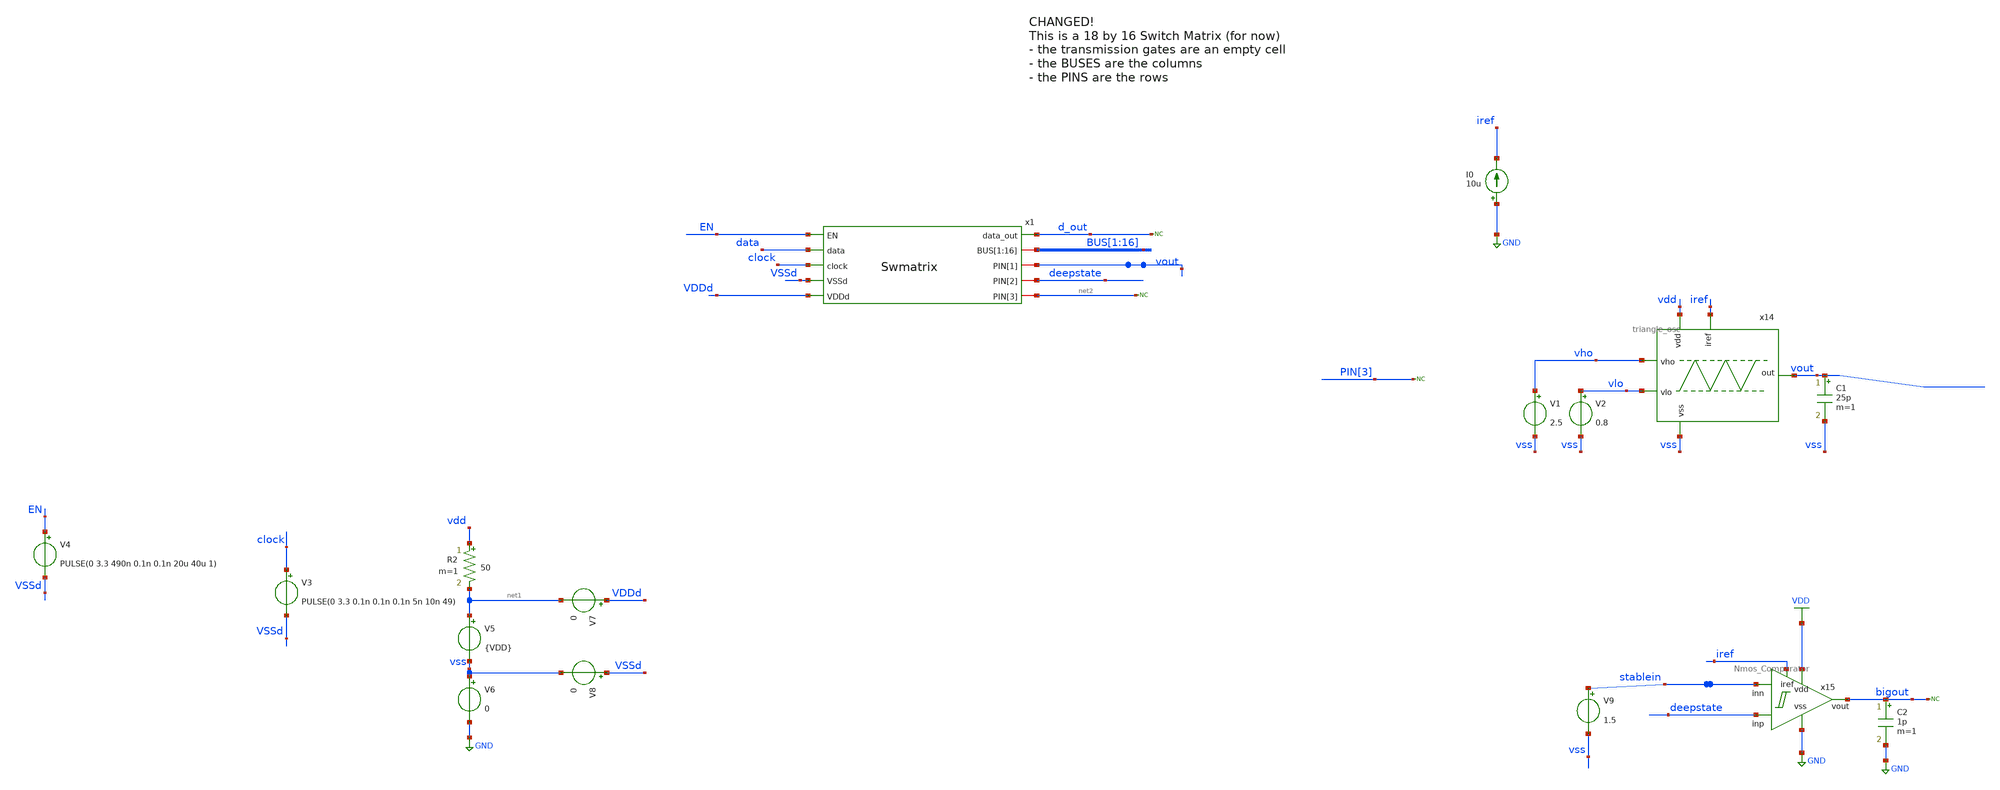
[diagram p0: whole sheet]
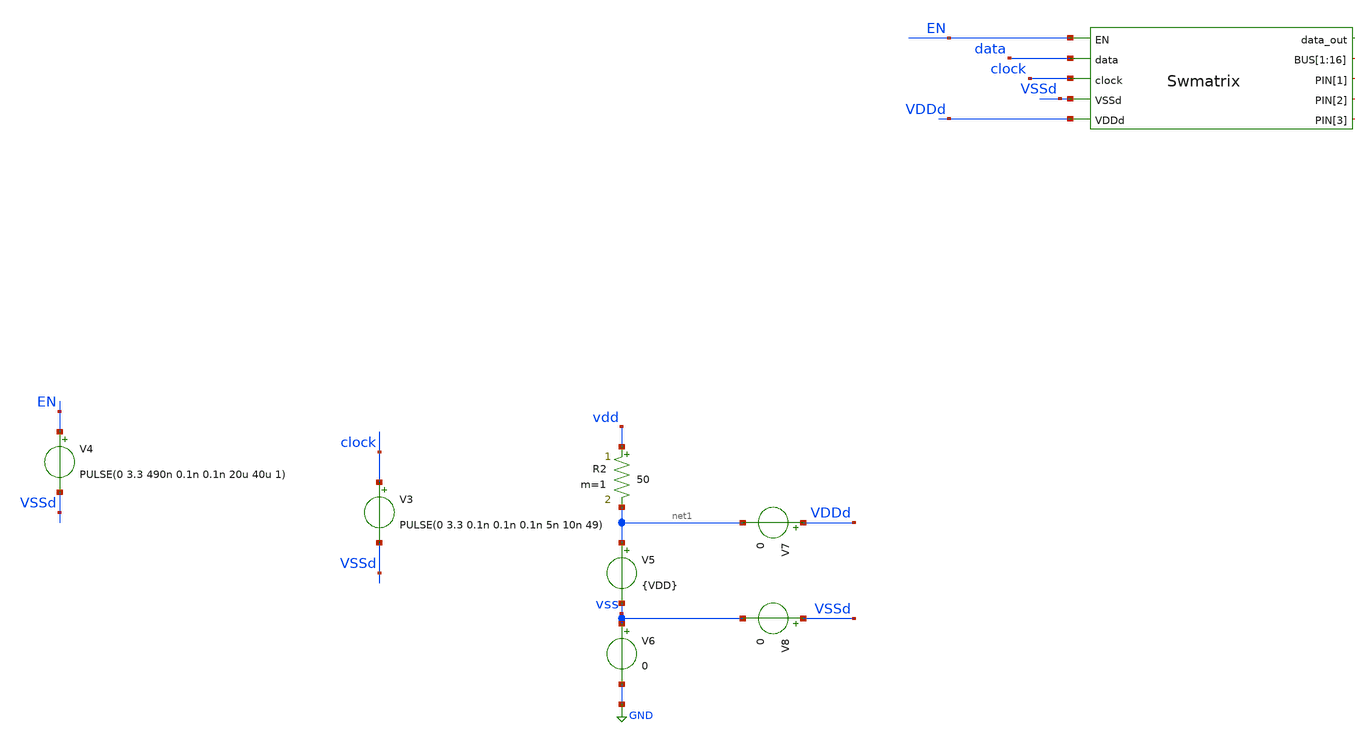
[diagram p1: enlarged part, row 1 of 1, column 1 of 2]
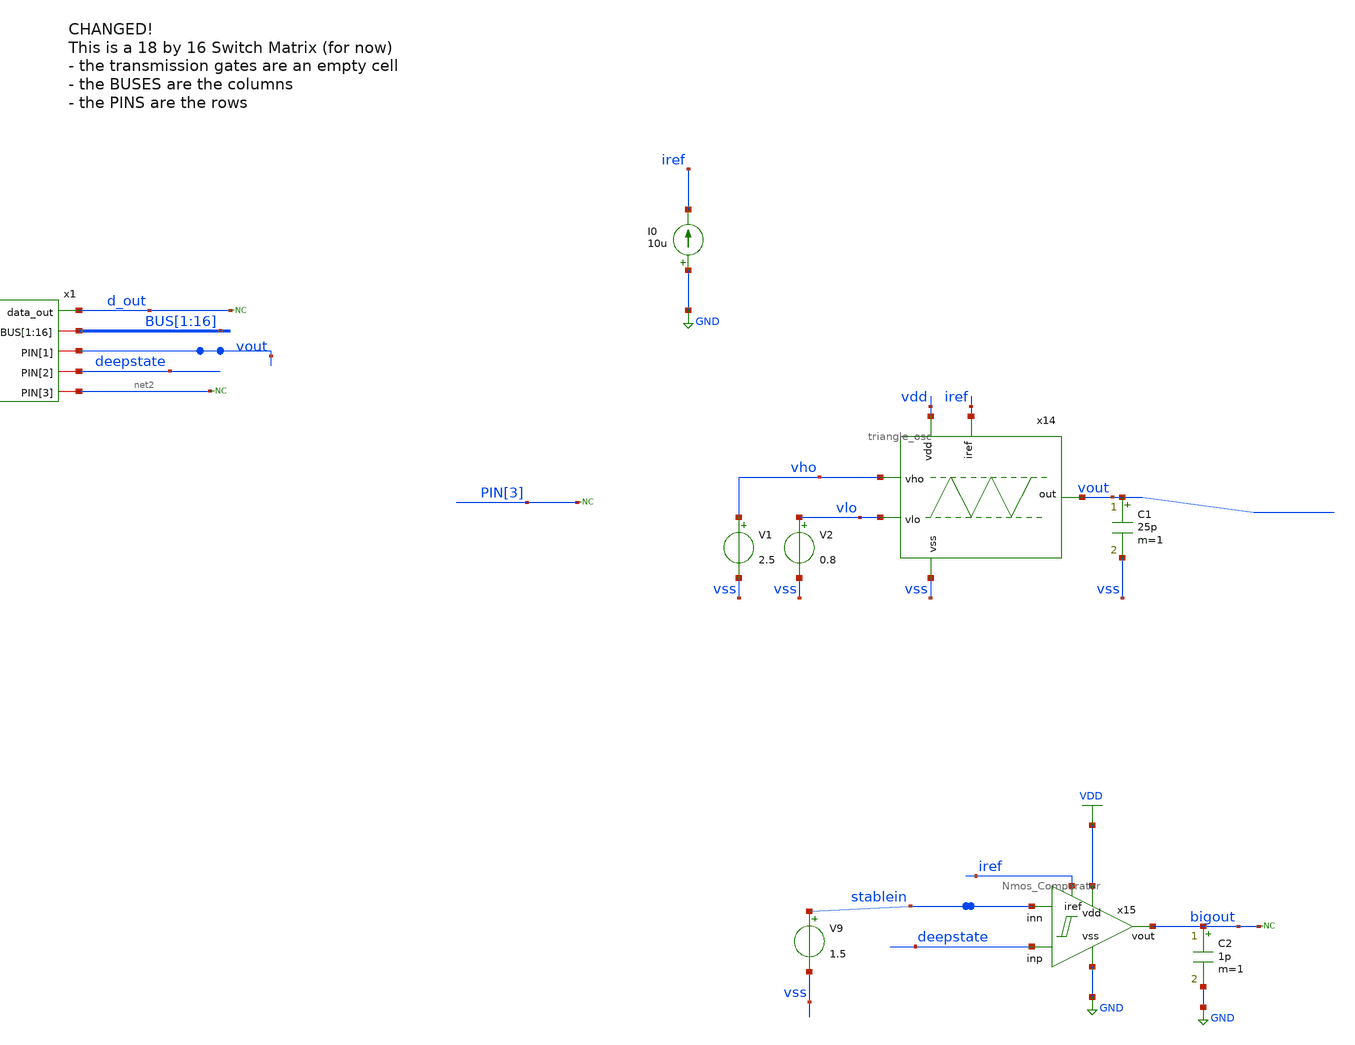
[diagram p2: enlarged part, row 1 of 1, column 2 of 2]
** sch_path: designs/savestate.sch
**.subckt savestate
* noconn d_out
V3 clock VSSd PULSE(0 3.3 0.1n 0.1n 0.1n 5n 10n 49)
V4 EN VSSd PULSE(0 3.3 490n 0.1n 0.1n 20u 40u 1)
V5 net1 vss {VDD}
V6 vss GND 0
V7 VDDd net1 0
V8 VSSd vss 0
R2 vdd net1 50 m=1
* noconn PIN[3]
x14 vdd vho vout vlo iref vss triangle_osc
V1 vho vss 2.5
V2 vlo vss 0.8
C1 vout vss 25p m=1
I0 GND iref 10u
* noconn bigout
x15 VDD bigout deepstate GND stablein iref Nmos_Comparator
C2 bigout GND 1p m=1
V9 stablein vss 1.5
x1 EN data d_out BUS[1] BUS[2] BUS[3] BUS[4] BUS[5] BUS[6] BUS[7] BUS[8] BUS[9] BUS[10] BUS[11]
+ BUS[12] BUS[13] BUS[14] BUS[15] BUS[16] vout clock VSSd VDDd deepstate net2 Swmatrix
* noconn #net2
**** begin user architecture code

.include /foss/pdks/gf180mcuD/libs.ref/gf180mcu_fd_sc_mcu9t5v0/spice/gf180mcu_fd_sc_mcu9t5v0.spice
.include $::180MCU_MODELS/design.ngspice
.lib $::180MCU_MODELS/sm141064.ngspice typical



.control

    save all
    TRAN 1n 20u
    write savestate.raw

.endc




.param VDD = 3.3
.param Tbit = 20n
.global VDDd VSSd
.ic v(vout)=0

* data
aclock [ clock_node ] clock_vector
.model clock_vector d_source(input_file="/foss/designs/libs/data_source/data_swmatrix_zeros.txt")
* convert digital signals to analog
aconvert [ clock_node ] [  data ] dac_in
.model dac_in dac_bridge (out_low=0V out_high=3.3V t_rise=0.1ns t_fall=0.1ns)


**** end user architecture code
**.ends
.GLOBAL GND
.GLOBAL VDD
.end
